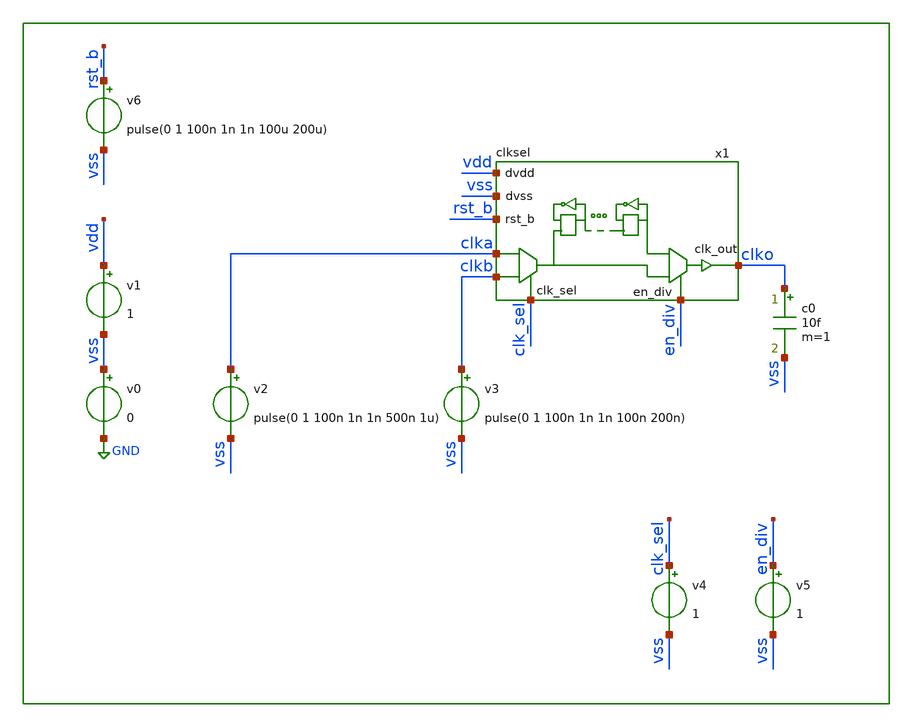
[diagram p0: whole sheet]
** sch_path: xschem/tb/clksel/tran_clksel.sch
**.subckt tran_clksel
v0 vss GND 0
v1 vdd vss 1
c0 clko vss 10f m=1
v2 clka vss pulse(0 1 100n 1n 1n 500n 1u)
x1 vdd vss rst_b clka clko clkb en_div clk_sel clksel
v3 clkb vss pulse(0 1 100n 1n 1n 100n 200n)
v4 clk_sel vss 1
v5 en_div vss 1
v6 rst_b vss pulse(0 1 100n 1n 1n 100u 200u)
**** begin user architecture code
.param MC_SWITCH=0

.include $::DESIGN_PATH/clksel/clksel.pex.sp

.control
tran 10e-9 10e-6
run
.endc


* FET CORNERS
.include $::SKYWATER_MODELS/corners/tt.spice
*.include $::SKYWATER_MODELS/corners/ff.spice
*.include $::SKYWATER_MODELS/corners/ss.spice
*.include $::SKYWATER_MODELS/corners/sf.spice
*.include $::SKYWATER_MODELS/corners/fs.spice

* TT + R + C
*.include $::SKYWATER_MODELS/corners/tt_rmax_cmax.spice
*.include $::SKYWATER_MODELS/corners/tt_rmin_cmin.spice
*.include $::SKYWATER_MODELS/corners/tt_rmax_cmin.spice
*.include $::SKYWATER_MODELS/corners/tt_rmin_cmax.spice

* FF + R + C
*.include $::SKYWATER_MODELS/corners/ff_rmax_cmax.spice
*.include $::SKYWATER_MODELS/corners/ff_rmin_cmin.spice
*.include $::SKYWATER_MODELS/corners/ff_rmax_cmin.spice
*.include $::SKYWATER_MODELS/corners/ff_rmin_cmax.spice


* SS + R + C
*.include $::SKYWATER_MODELS/corners/ss_rmax_cmax.spice
*.include $::SKYWATER_MODELS/corners/ss_rmin_cmin.spice
*.include $::SKYWATER_MODELS/corners/ss_rmax_cmin.spice
*.include $::SKYWATER_MODELS/corners/ss_rmin_cmax.spice

* SF + R + C
*.include $::SKYWATER_MODELS/corners/sf_rmax_cmax.spice
*.include $::SKYWATER_MODELS/corners/sf_rmin_cmin.spice
*.include $::SKYWATER_MODELS/corners/sf_rmax_cmin.spice
*.include $::SKYWATER_MODELS/corners/sf_rmin_cmax.spice

* FS + R + C
*.include $::SKYWATER_MODELS/corners/fs_rmax_cmax.spice
*.include $::SKYWATER_MODELS/corners/fs_rmin_cmin.spice
*.include $::SKYWATER_MODELS/corners/fs_rmax_cmin.spice
*.include $::SKYWATER_MODELS/corners/fs_rmin_cmax.spice

**** end user architecture code
**.ends

* expanding   symbol:  clksel/clksel.sym # of pins=8
** sym_path: xschem/clksel/clksel.sym
** sch_path: xschem/clksel/clksel.sch
.subckt clksel dvdd dvss rst_b clk_int clk_out clk_ext en_div clk_sel
*.ipin clk_int
*.ipin rst_b
*.opin clk_out
*.iopin dvdd
*.iopin dvss
*.ipin clk_ext
*.ipin en_div
*.ipin clk_sel
x1 dvss net2 net3 rst_b dvdd clkdiv
x2 clk_int clk_ext clk_sel dvss dvss dvdd dvdd net2 sky130_fd_sc_hd__mux2_2
x3 net1 dvss dvss dvdd dvdd clk_out sky130_fd_sc_hd__clkbuf_8
x4 net2 net3 en_div dvss dvss dvdd dvdd net1 sky130_fd_sc_hd__mux2_2
.ends


* expanding   symbol:  clkdiv/clkdiv.sym # of pins=5
** sym_path: xschem/clkdiv/clkdiv.sym
** sch_path: xschem/clkdiv/clkdiv.sch
.subckt clkdiv dvss in out rst_b dvdd
*.ipin in
*.ipin rst_b
*.opin out
*.iopin dvdd
*.iopin dvss
x6 in net1 rst_b dvss dvss dvdd dvdd div2 net5 sky130_fd_sc_hd__dfrbp_1
x8 div2 dvss dvss dvdd dvdd net1 sky130_fd_sc_hd__inv_1
* noconn #net5
x1 div2 net2 rst_b dvss dvss dvdd dvdd div4 net6 sky130_fd_sc_hd__dfrbp_1
x2 div4 dvss dvss dvdd dvdd net2 sky130_fd_sc_hd__inv_1
* noconn #net6
x3 div4 net3 rst_b dvss dvss dvdd dvdd div8 net7 sky130_fd_sc_hd__dfrbp_1
x4 div8 dvss dvss dvdd dvdd net3 sky130_fd_sc_hd__inv_1
* noconn #net7
x5 div8 net4 rst_b dvss dvss dvdd dvdd out net8 sky130_fd_sc_hd__dfrbp_1
x7 out dvss dvss dvdd dvdd net4 sky130_fd_sc_hd__inv_1
* noconn #net8
xdec[7] dvss dvss dvdd dvdd sky130_fd_sc_hd__decap_4
xdec[6] dvss dvss dvdd dvdd sky130_fd_sc_hd__decap_4
xdec[5] dvss dvss dvdd dvdd sky130_fd_sc_hd__decap_4
xdec[4] dvss dvss dvdd dvdd sky130_fd_sc_hd__decap_4
xdec[3] dvss dvss dvdd dvdd sky130_fd_sc_hd__decap_4
xdec[2] dvss dvss dvdd dvdd sky130_fd_sc_hd__decap_4
xdec[1] dvss dvss dvdd dvdd sky130_fd_sc_hd__decap_4
xdec[0] dvss dvss dvdd dvdd sky130_fd_sc_hd__decap_4
xtap dvss dvdd sky130_fd_sc_hd__tapvpwrvgnd_1
.ends

.GLOBAL GND
**** begin user architecture code
[sky130_models]

**** end user architecture code
.end
